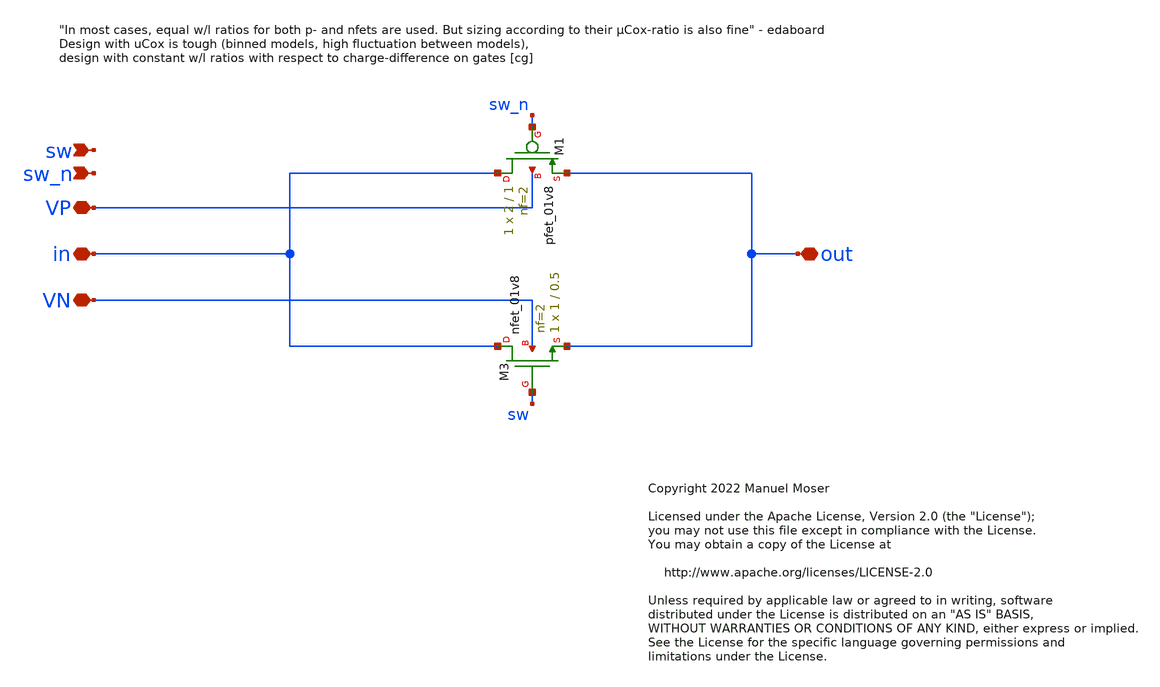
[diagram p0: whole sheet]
** sch_path: xschem/adc_vcm_switch.sch
* Copyright 2022 Manuel Moser
* Licensed under the Apache License, Version 2.0 (the "License");
**.subckt adc_vcm_switch VN VP sw_n sw in out
*.iopin VN
*.iopin VP
*.ipin sw_n
*.ipin sw
*.iopin in
*.iopin out
XM1 in sw_n out VP sky130_fd_pr__pfet_01v8 L=1 W=2 nf=2 ad='int((nf+1)/2) * W/nf * 0.29' as='int((nf+2)/2) * W/nf * 0.29'
+ pd='2*int((nf+1)/2) * (W/nf + 0.29)' ps='2*int((nf+2)/2) * (W/nf + 0.29)' nrd='0.29 / W' nrs='0.29 / W'
+ sa=0 sb=0 sd=0 mult=1 m=1
XM3 in sw out VN sky130_fd_pr__nfet_01v8 L=0.5 W=1 nf=2 ad='int((nf+1)/2) * W/nf * 0.29' as='int((nf+2)/2) * W/nf * 0.29'
+ pd='2*int((nf+1)/2) * (W/nf + 0.29)' ps='2*int((nf+2)/2) * (W/nf + 0.29)' nrd='0.29 / W' nrs='0.29 / W'
+ sa=0 sb=0 sd=0 mult=1 m=1
**.ends
.end
